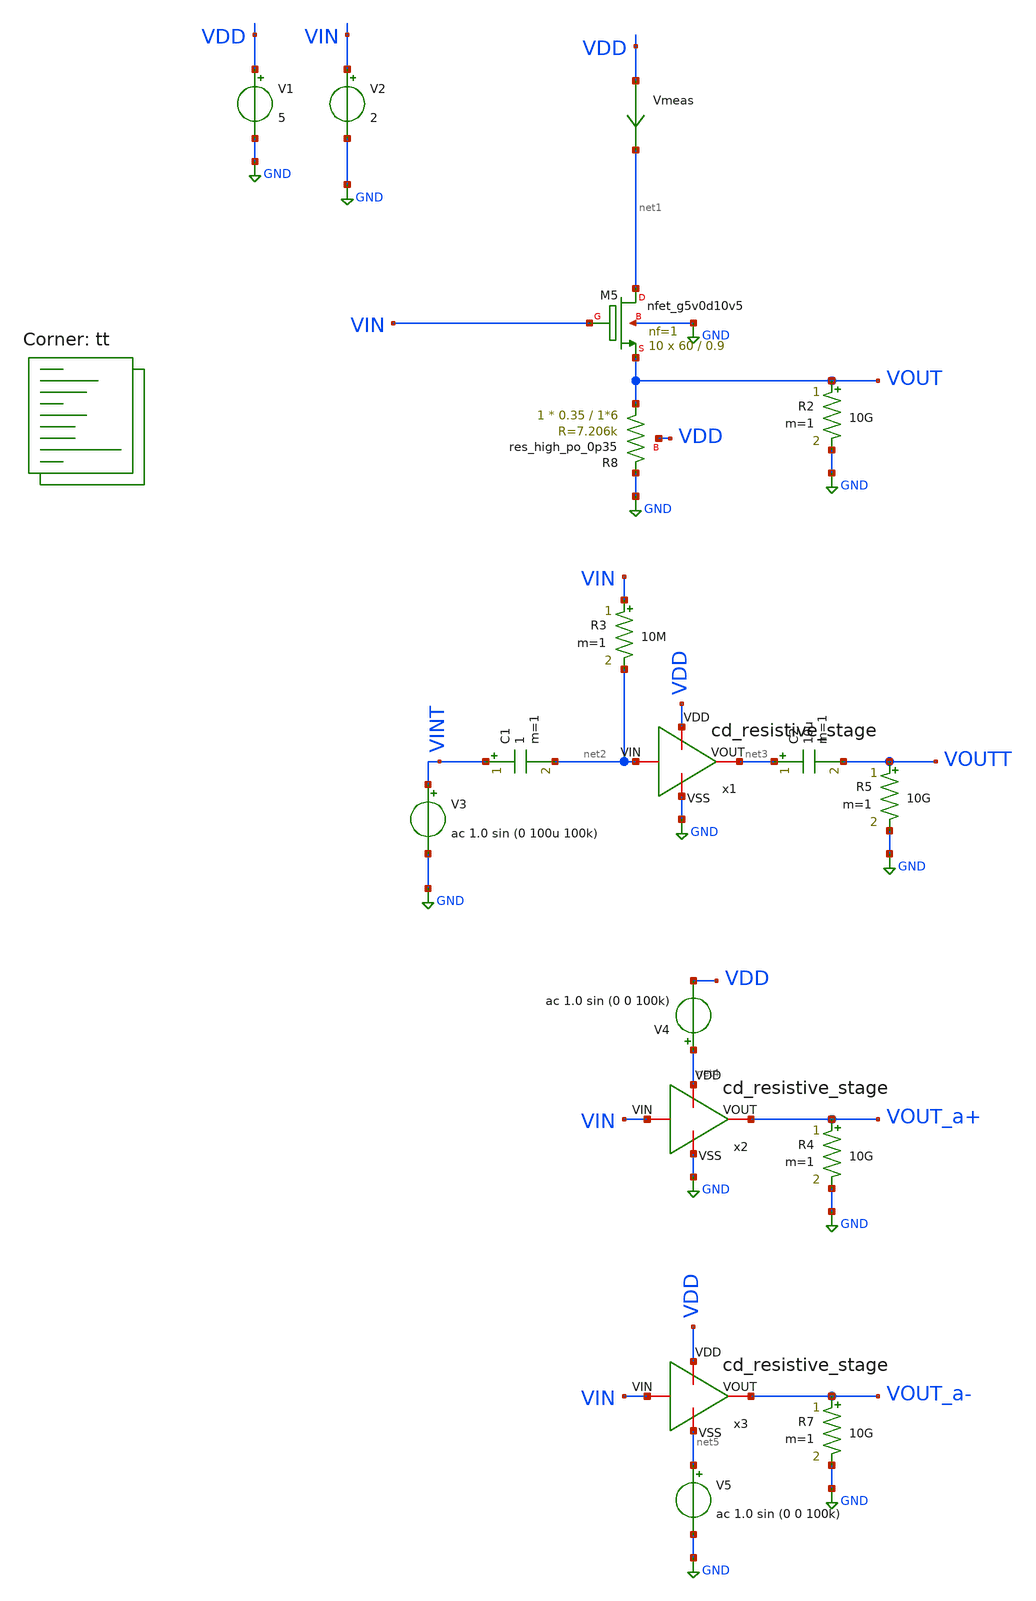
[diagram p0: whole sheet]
** sch_path: amplifiers/single_stage_amps/basic_stages/cd_resistive_stage/cd_resistive_stage_test.sch
**.subckt cd_resistive_stage_test
Vmeas VDD net1 0
.save i(vmeas)
V1 VDD GND 5
V2 VIN GND 2
V3 VINT GND ac 1.0 sin (0 100u 100k)
R2 VOUT GND 10G m=1
C1 VINT net2 1 m=1
R3 VIN net2 10M m=1
R5 VOUTT GND 10G m=1
C2 net3 VOUTT 10u m=1
R4 VOUT_a+ GND 10G m=1
V4 net4 VDD ac 1.0 sin (0 0 100k)
R7 VOUT_a- GND 10G m=1
V5 net5 GND ac 1.0 sin (0 0 100k)
XR8 VOUT GND VDD sky130_fd_pr__res_high_po_0p35 L=1*6 mult=1 m=1
XM5 net1 VIN VOUT GND sky130_fd_pr__nfet_g5v0d10v5 L=0.9 W=60 nf=1 ad='int((1 + 1)/2) * 60 / 1 * 0.29'
+ as='int((1 + 2)/2) * 60 / 1 * 0.29' pd='2*int((1 + 1)/2) * (60 / 1 + 0.29)' ps='2*int((1 + 2)/2) * (60 / 1 + 0.29)'
+ nrd='0.29 / 60 ' nrs='0.29 / 60 ' sa=0 sb=0 sd=0 mult=10 m=10
x1 VDD GND net2 net3 cd_resistive_stage
x2 net4 GND VIN VOUT_a+ cd_resistive_stage
x3 VDD net5 VIN VOUT_a- cd_resistive_stage
**** begin user architecture code

**************************************************************
**************************************************************
**************************************************************
**************************************************************
**************************************************************
*LIBs*********************************************************
**************************************************************
**************************************************************
**************************************************************
**************************************************************
**************************************************************
*.lib $::SKYWATER_MODELS/sky130.lib.spice tt
* chose the corners in the corner file
* tt_mm for mismatch
* ss ff sf fs standart corners
* ll hh lh hl capacitor and resistors corners
* mc for total process variation including corners
**************************************************************
**************************************************************
**************************************************************
**************************************************************
**************************************************************
*Corners/montecarlo options***********************************
**************************************************************
**************************************************************
**************************************************************
**************************************************************
**************************************************************
.TEMP 27
**************************************************************
**************************************************************
**************************************************************
**************************************************************
*SIMULATION and Plots*****************************************
**************************************************************
**************************************************************
**************************************************************
**************************************************************
.control
save all
dc V2 0 5 0.01
*dc simulation
plot v(VOUT) v(VIN) deriv(v(VOUT))
*ploting VIN VOUT and the voltage gain
plot i(Vmeas)
*ploting the current for curiosity
tran 0.1ns 20u
*transient simulation
plot (v(VINT)) (v(VOUTT))
*simple plot to exemplify the gain
fft v(VOUTT) v(VINT)
*fast fourier transfor
plot mag(v(VOUTT)) mag(v(VINT))
* analyse the frequency spectrum of the transient waves, to detect distortion
ac dec 20 1 50G
*simple ac simulation
plot db(v(VOUTT))
plot db(v(VOUT_a+))
plot db(v(VOUT_a-))
*gain in function of the input frequency
.endc

.lib $::SKYWATER_MODELS/sky130.lib.spice tt

** Additional definitions for NPN
.param  dkisnpn1x1=8.7913e-01 dkbfnpn1x1=9.8501e-01  dkisnpn1x2=9.0950e-01 dkbfnpn1x2=9.6759e-01
+  dkisnpnpolyhv=1.0 dkbfnpnpolyhv=1.0


**** end user architecture code
**.ends

* expanding   symbol:
*+  /home/vasco/Desktop/sky130A/amplifiers/single_stage_amps/basic_stages/cd_resistive_stage/cd_resistive_stage.sym # of pins=4
** sym_path: amplifiers/single_stage_amps/basic_stages/cd_resistive_stage/cd_resistive_stage.sym
** sch_path: amplifiers/single_stage_amps/basic_stages/cd_resistive_stage/cd_resistive_stage.sch
.subckt cd_resistive_stage VDD VSS VIN VOUT
*.iopin VDD
*.iopin VSS
*.iopin VIN
*.iopin VOUT
XR8 VOUT VSS VDD sky130_fd_pr__res_high_po_0p35 L=1*6 mult=1 m=1
XM5 VDD VIN VOUT VSS sky130_fd_pr__nfet_g5v0d10v5 L=0.9 W=60 nf=1 ad='int((1 + 1)/2) * 60 / 1 * 0.29'
+ as='int((1 + 2)/2) * 60 / 1 * 0.29' pd='2*int((1 + 1)/2) * (60 / 1 + 0.29)' ps='2*int((1 + 2)/2) * (60 / 1 + 0.29)'
+ nrd='0.29 / 60 ' nrs='0.29 / 60 ' sa=0 sb=0 sd=0 mult=10 m=10
.ends

.GLOBAL GND
.end
